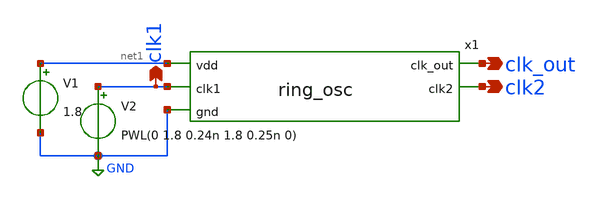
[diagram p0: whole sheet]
** sch_path: week4/xschem/ring/ring_osc_tb.sch
**.subckt ring_osc_tb clk_out clk1 clk2
*.opin clk_out
*.opin clk1
*.opin clk2
x1 net1 clk_out clk1 clk2 GND ring_osc
V1 net1 GND 1.8
V2 clk1 GND PWL(0 1.8 0.24n 1.8 0.25n 0)
**** begin user architecture code


.lib /usr/local/share/pdk/sky130A/libs.tech/ngspice/sky130.lib.spice tt
.control
	tran 0.01n 2n
	plot v(clk1) v(clk_out)
.endc
.save all


**** end user architecture code
**.ends

* expanding   symbol:  ring_osc.sym # of pins=5
** sym_path: week4/xschem/ring/ring_osc.sym
** sch_path: week4/xschem/ring/ring_osc.sch
.subckt ring_osc vdd clk_out clk1 clk2 gnd
*.ipin vdd
*.ipin gnd
*.ipin clk1
*.opin clk_out
*.opin clk2
XM7 vdd clk1 net1 gnd sky130_fd_pr__nfet_01v8 L=0.15 W=1 nf=1 ad='int((nf+1)/2) * W/nf * 0.29' as='int((nf+2)/2) * W/nf * 0.29'
+ pd='2*int((nf+1)/2) * (W/nf + 0.29)' ps='2*int((nf+2)/2) * (W/nf + 0.29)' nrd='0.29 / W' nrs='0.29 / W'
+ sa=0 sb=0 sd=0 mult=1 m=1
XM8 clk2 clk1 gnd gnd sky130_fd_pr__nfet_01v8 L=0.15 W=1 nf=1 ad='int((nf+1)/2) * W/nf * 0.29' as='int((nf+2)/2) * W/nf * 0.29'
+ pd='2*int((nf+1)/2) * (W/nf + 0.29)' ps='2*int((nf+2)/2) * (W/nf + 0.29)' nrd='0.29 / W' nrs='0.29 / W'
+ sa=0 sb=0 sd=0 mult=1 m=1
XM9 clk2 clk1 vdd vdd sky130_fd_pr__pfet_01v8 L=0.15 W=1 nf=1 ad='int((nf+1)/2) * W/nf * 0.29' as='int((nf+2)/2) * W/nf * 0.29'
+ pd='2*int((nf+1)/2) * (W/nf + 0.29)' ps='2*int((nf+2)/2) * (W/nf + 0.29)' nrd='0.29 / W' nrs='0.29 / W'
+ sa=0 sb=0 sd=0 mult=1 m=1
XM10 clk_out clk2 net1 gnd sky130_fd_pr__nfet_01v8 L=0.15 W=1 nf=1 ad='int((nf+1)/2) * W/nf * 0.29' as='int((nf+2)/2) * W/nf * 0.29'
+ pd='2*int((nf+1)/2) * (W/nf + 0.29)' ps='2*int((nf+2)/2) * (W/nf + 0.29)' nrd='0.29 / W' nrs='0.29 / W'
+ sa=0 sb=0 sd=0 mult=1 m=1
x1 vdd gnd clk_out net1 sub_comp
.ends


* expanding   symbol:  sub_comp.sym # of pins=4
** sym_path: week4/xschem/ring/sub_comp.sym
** sch_path: week4/xschem/ring/sub_comp.sch
.subckt sub_comp vdd gnd clkout clkin
*.ipin clkin
*.opin clkout
*.ipin vdd
*.ipin gnd
XM1 net1 clkin gnd gnd sky130_fd_pr__nfet_01v8 L=0.15 W=1 nf=1 ad='int((nf+1)/2) * W/nf * 0.29' as='int((nf+2)/2) * W/nf * 0.29'
+ pd='2*int((nf+1)/2) * (W/nf + 0.29)' ps='2*int((nf+2)/2) * (W/nf + 0.29)' nrd='0.29 / W' nrs='0.29 / W'
+ sa=0 sb=0 sd=0 mult=1 m=1
XM2 net1 clkin vdd vdd sky130_fd_pr__pfet_01v8 L=0.15 W=3 nf=1 ad='int((nf+1)/2) * W/nf * 0.29' as='int((nf+2)/2) * W/nf * 0.29'
+ pd='2*int((nf+1)/2) * (W/nf + 0.29)' ps='2*int((nf+2)/2) * (W/nf + 0.29)' nrd='0.29 / W' nrs='0.29 / W'
+ sa=0 sb=0 sd=0 mult=1 m=1
XM3 net2 net1 gnd gnd sky130_fd_pr__nfet_01v8 L=0.15 W=1 nf=1 ad='int((nf+1)/2) * W/nf * 0.29' as='int((nf+2)/2) * W/nf * 0.29'
+ pd='2*int((nf+1)/2) * (W/nf + 0.29)' ps='2*int((nf+2)/2) * (W/nf + 0.29)' nrd='0.29 / W' nrs='0.29 / W'
+ sa=0 sb=0 sd=0 mult=1 m=1
XM4 net2 net1 vdd vdd sky130_fd_pr__pfet_01v8 L=0.15 W=6 nf=1 ad='int((nf+1)/2) * W/nf * 0.29' as='int((nf+2)/2) * W/nf * 0.29'
+ pd='2*int((nf+1)/2) * (W/nf + 0.29)' ps='2*int((nf+2)/2) * (W/nf + 0.29)' nrd='0.29 / W' nrs='0.29 / W'
+ sa=0 sb=0 sd=0 mult=1 m=1
XM7 clkout net3 gnd gnd sky130_fd_pr__nfet_01v8 L=0.15 W=1 nf=1 ad='int((nf+1)/2) * W/nf * 0.29' as='int((nf+2)/2) * W/nf * 0.29'
+ pd='2*int((nf+1)/2) * (W/nf + 0.29)' ps='2*int((nf+2)/2) * (W/nf + 0.29)' nrd='0.29 / W' nrs='0.29 / W'
+ sa=0 sb=0 sd=0 mult=1 m=1
XM8 clkout net3 vdd vdd sky130_fd_pr__pfet_01v8 L=0.15 W=96 nf=2 ad='int((nf+1)/2) * W/nf * 0.29' as='int((nf+2)/2) * W/nf * 0.29'
+ pd='2*int((nf+1)/2) * (W/nf + 0.29)' ps='2*int((nf+2)/2) * (W/nf + 0.29)' nrd='0.29 / W' nrs='0.29 / W'
+ sa=0 sb=0 sd=0 mult=1 m=1
XM5 net4 net2 gnd gnd sky130_fd_pr__nfet_01v8 L=0.15 W=1 nf=1 ad='int((nf+1)/2) * W/nf * 0.29' as='int((nf+2)/2) * W/nf * 0.29'
+ pd='2*int((nf+1)/2) * (W/nf + 0.29)' ps='2*int((nf+2)/2) * (W/nf + 0.29)' nrd='0.29 / W' nrs='0.29 / W'
+ sa=0 sb=0 sd=0 mult=1 m=1
XM6 net4 net2 vdd vdd sky130_fd_pr__pfet_01v8 L=0.15 W=12 nf=1 ad='int((nf+1)/2) * W/nf * 0.29' as='int((nf+2)/2) * W/nf * 0.29'
+ pd='2*int((nf+1)/2) * (W/nf + 0.29)' ps='2*int((nf+2)/2) * (W/nf + 0.29)' nrd='0.29 / W' nrs='0.29 / W'
+ sa=0 sb=0 sd=0 mult=1 m=1
XM9 net5 net4 gnd gnd sky130_fd_pr__nfet_01v8 L=0.15 W=1 nf=1 ad='int((nf+1)/2) * W/nf * 0.29' as='int((nf+2)/2) * W/nf * 0.29'
+ pd='2*int((nf+1)/2) * (W/nf + 0.29)' ps='2*int((nf+2)/2) * (W/nf + 0.29)' nrd='0.29 / W' nrs='0.29 / W'
+ sa=0 sb=0 sd=0 mult=1 m=1
XM10 net5 net4 vdd vdd sky130_fd_pr__pfet_01v8 L=0.15 W=24 nf=1 ad='int((nf+1)/2) * W/nf * 0.29' as='int((nf+2)/2) * W/nf * 0.29'
+ pd='2*int((nf+1)/2) * (W/nf + 0.29)' ps='2*int((nf+2)/2) * (W/nf + 0.29)' nrd='0.29 / W' nrs='0.29 / W'
+ sa=0 sb=0 sd=0 mult=1 m=1
XM11 net6 net5 gnd gnd sky130_fd_pr__nfet_01v8 L=0.15 W=1 nf=1 ad='int((nf+1)/2) * W/nf * 0.29' as='int((nf+2)/2) * W/nf * 0.29'
+ pd='2*int((nf+1)/2) * (W/nf + 0.29)' ps='2*int((nf+2)/2) * (W/nf + 0.29)' nrd='0.29 / W' nrs='0.29 / W'
+ sa=0 sb=0 sd=0 mult=1 m=1
XM12 net6 net5 vdd vdd sky130_fd_pr__pfet_01v8 L=0.15 W=48 nf=1 ad='int((nf+1)/2) * W/nf * 0.29' as='int((nf+2)/2) * W/nf * 0.29'
+ pd='2*int((nf+1)/2) * (W/nf + 0.29)' ps='2*int((nf+2)/2) * (W/nf + 0.29)' nrd='0.29 / W' nrs='0.29 / W'
+ sa=0 sb=0 sd=0 mult=1 m=1
XM13 net3 net6 gnd gnd sky130_fd_pr__nfet_01v8 L=0.15 W=1 nf=1 ad='int((nf+1)/2) * W/nf * 0.29' as='int((nf+2)/2) * W/nf * 0.29'
+ pd='2*int((nf+1)/2) * (W/nf + 0.29)' ps='2*int((nf+2)/2) * (W/nf + 0.29)' nrd='0.29 / W' nrs='0.29 / W'
+ sa=0 sb=0 sd=0 mult=1 m=1
XM14 net3 net6 vdd vdd sky130_fd_pr__pfet_01v8 L=0.15 W=96 nf=1 ad='int((nf+1)/2) * W/nf * 0.29' as='int((nf+2)/2) * W/nf * 0.29'
+ pd='2*int((nf+1)/2) * (W/nf + 0.29)' ps='2*int((nf+2)/2) * (W/nf + 0.29)' nrd='0.29 / W' nrs='0.29 / W'
+ sa=0 sb=0 sd=0 mult=1 m=1
.ends

.GLOBAL GND
.end
